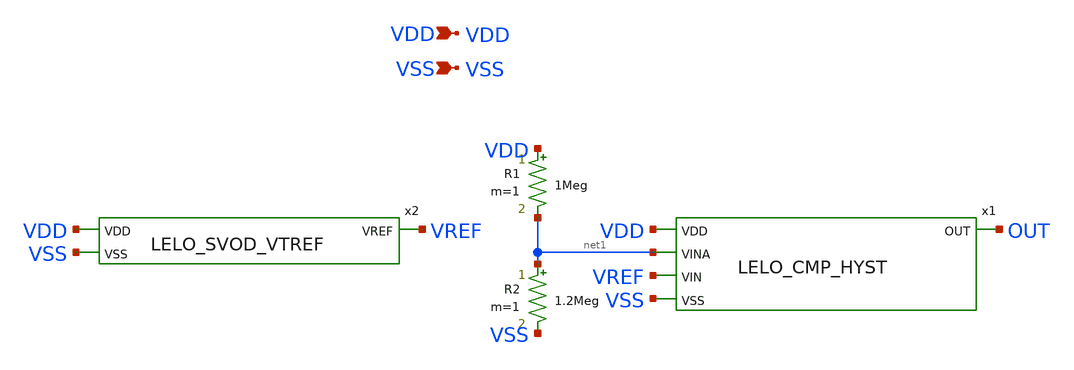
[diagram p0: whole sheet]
** sch_path: design/LELO_SVOD_SKY130A/LELO_STARTUP_DETECTOR_TEST.sch
**.subckt LELO_STARTUP_DETECTOR_TEST VDD VSS
*.ipin VDD
*.ipin VSS
x1 VDD OUT net1 VREF VSS LELO_CMP_HYST
x2 VDD VSS VREF LELO_SVOD_VTREF
R1 VDD net1 1Meg m=1
R2 net1 VSS 1.2Meg m=1
**.ends
.end
